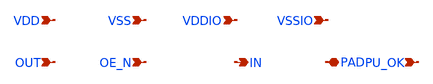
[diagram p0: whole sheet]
** sch_path: sch/pads/gf180mcuD/sdr_bidir_pad.sch
**.subckt sdr_bidir_pad OUT OE_N IN PAD PU_OK VDD VSS VDDIO VSSIO
*.ipin OUT
*.ipin OE_N
*.opin IN
*.iopin PAD
*.ipin PU_OK
*.ipin VDD
*.ipin VSS
*.ipin VDDIO
*.ipin VSSIO
**** begin user architecture code


* GENERATED by generator/emit_pads.py -- DO NOT EDIT BY HAND
* backend: gf180mcuD   pdk: gf180mcuD
* topology: specs/pads/topology.yaml v1 -- ONE shared schematic, only device names change
* STATUS: topology_template_only
* license: Apache-2.0 (GlobalFoundries PDK Authors, design.ngspice header)
* SIZE UNITS: topology params are metres; nfet_03v3/pfet_03v3 take w/l in metres
* ESD NOTE: 2-terminal .model diodes; area unit and orientation still need schematic review
*
* NOT SIMULATABLE. This is a TOPOLOGY TEMPLATE:
*   - every W / L / NF / R / area is an unresolved parameter
*     (see required_params.json). ngspice rejects them until filled.
*   - PAD_OE_CTRL is a generated transistor-level block (IO gates plus
*     an optional core-to-IO level shifter); its devices reuse the
*     pre-driver sizing placeholders and are not optimized.
*   - diode orientation, bulk ties and the series-R third terminal must
*     be confirmed at schematic review; they are NOT signed off here.
*   - L_R_SERIES is the on-chip resistor LENGTH. The target
*     resistance in ohm is a board-level SI input, not a pad param;
*     converting target R to L needs a per-PDK sheet resistance.
*
* Device-instantiation syntax is per backend (nf vs ng, m vs mr,
* r_length/r_width vs w/l, 2-terminal diode model vs 3-terminal ESD
* subckt). It lives in specs/pads/devices/<backend>.yaml; the block
* topology below stays shared.
*
* Expected includes (NOT bundled; integrator supplies models.spice):
*   libs.tech/ngspice/sm141064.ngspice
*   libs.tech/ngspice/design.ngspice
*
* Shared signal chain (docs/ARCHITECTURE.md section 5):
*   OUT/OE_N --[level shift if VDD != VDDIO]--> pre-driver --> tri-state
*   --> series R --> PAD --> ESD (to VDDIO / VSSIO + power clamp)
*   PAD --> CMOS/Schmitt RX --> [level shift back] --> IN
*   power-up Hi-Z until VDD and VDDIO are both present (PU_OK)

X_INV_P Y A VDDIO VDDIO pfet_03v3 w=W_P_PDRV l=L_PDRV nf=NF_DEVICE m=M_DEVICE
X_INV_N Y A VSSIO VSSIO nfet_03v3 w=W_N_PDRV l=L_PDRV nf=NF_DEVICE m=M_DEVICE
X_NAND_P1 Y A VDDIO VDDIO pfet_03v3 w=W_P_PDRV l=L_PDRV nf=NF_DEVICE m=M_DEVICE
X_NAND_P2 Y B VDDIO VDDIO pfet_03v3 w=W_P_PDRV l=L_PDRV nf=NF_DEVICE m=M_DEVICE
X_NAND_N1 Y A nand_mid VSSIO nfet_03v3 w=W_N_PDRV l=L_PDRV nf=NF_DEVICE m=M_DEVICE
X_NAND_N2 nand_mid B VSSIO VSSIO nfet_03v3 w=W_N_PDRV l=L_PDRV nf=NF_DEVICE m=M_DEVICE
X_NOR_P1 Y A nor_mid VDDIO pfet_03v3 w=W_P_PDRV l=L_PDRV nf=NF_DEVICE m=M_DEVICE
X_NOR_P2 nor_mid B VDDIO VDDIO pfet_03v3 w=W_P_PDRV l=L_PDRV nf=NF_DEVICE m=M_DEVICE
X_NOR_N1 Y A VSSIO VSSIO nfet_03v3 w=W_N_PDRV l=L_PDRV nf=NF_DEVICE m=M_DEVICE
X_NOR_N2 Y B VSSIO VSSIO nfet_03v3 w=W_N_PDRV l=L_PDRV nf=NF_DEVICE m=M_DEVICE
* core_v == vddio_v: OUT is already IO domain
V_OUT_I OUT_I OUT 0
X_INV_O OUT OUTB_I VDDIO VSSIO INV_IO
* OE_N and PU_OK are IO-domain control inputs in this macro
X_INV_OE OE_N OENB VDDIO VSSIO INV_IO
X_NAND PU_OK OENB EN_N VDDIO VSSIO NAND2_IO
X_NOR_GN EN_N OUT_I N_GN VDDIO VSSIO NOR2_IO
X_NOR_GP EN_N OUTB_I NGPB VDDIO VSSIO NOR2_IO
X_INV_NGP NGPB N_GP VDDIO VSSIO INV_IO

* --- core_v == vddio_v: NO level shifter (Nominal core and IO voltages are equal; ARCHITECTURE.md
*+ section 5.1 says no level shift. Pre-driver still required.) ---
* OUT / OE_N are already at IO-domain levels; pre-driver still required.

* --- OE / power-up gating: real transistor-level block (see header) ---
X_OE_CTRL n_gp n_gn OUT OE_N PU_OK VDD VSS VDDIO VSSIO PAD_OE_CTRL

* --- pre-driver chain (even stage count preserves polarity) ---
X_PDRV_P_GP1 n_gp_s1 n_gp VDDIO VDDIO pfet_03v3 w=W_P_PDRV l=L_PDRV nf=NF_DEVICE m=M_DEVICE
X_PDRV_N_GP1 n_gp_s1 n_gp VSSIO VSSIO nfet_03v3 w=W_N_PDRV l=L_PDRV nf=NF_DEVICE m=M_DEVICE
X_PDRV_P_GP2 n_gp_drv n_gp_s1 VDDIO VDDIO pfet_03v3 w=W_P_PDRV l=L_PDRV nf=NF_DEVICE m=M_DEVICE
X_PDRV_N_GP2 n_gp_drv n_gp_s1 VSSIO VSSIO nfet_03v3 w=W_N_PDRV l=L_PDRV nf=NF_DEVICE m=M_DEVICE
X_PDRV_P_GN1 n_gn_s1 n_gn VDDIO VDDIO pfet_03v3 w=W_P_PDRV l=L_PDRV nf=NF_DEVICE m=M_DEVICE
X_PDRV_N_GN1 n_gn_s1 n_gn VSSIO VSSIO nfet_03v3 w=W_N_PDRV l=L_PDRV nf=NF_DEVICE m=M_DEVICE
X_PDRV_P_GN2 n_gn_drv n_gn_s1 VDDIO VDDIO pfet_03v3 w=W_P_PDRV l=L_PDRV nf=NF_DEVICE m=M_DEVICE
X_PDRV_N_GN2 n_gn_drv n_gn_s1 VSSIO VSSIO nfet_03v3 w=W_N_PDRV l=L_PDRV nf=NF_DEVICE m=M_DEVICE

* --- tri-state output (PMOS to VDDIO, NMOS to VSSIO) ---
X_OUT_P n_pre n_gp_drv VDDIO VDDIO pfet_03v3 w=W_P_OUT l=L_P_OUT nf=NF_P_OUT m=M_DEVICE
X_OUT_N n_pre n_gn_drv VSSIO VSSIO nfet_03v3 w=W_N_OUT l=L_N_OUT nf=NF_N_OUT m=M_DEVICE

* --- on-chip series damping resistor (may instead live on the board) ---
X_RSER n_pre PAD VSSIO ppolyf_u r_length=L_R_SERIES r_width=W_R_SERIES

* --- ESD: primary diodes + VDDIO-to-VSSIO clamp ---
D_ESD_UP PAD VDDIO diode_pd2nw_03v3 area=ESD_AREA_UP
D_ESD_DN VSSIO PAD diode_nd2ps_03v3 area=ESD_AREA_DN
D_CLAMP VSSIO VDDIO diode_pd2nw_03v3 area=ESD_CLAMP_W

* --- SDR receiver: thick-oxide CMOS inverter (Schmitt optional) ---
X_RX_N IN PAD VSSIO VSSIO nfet_03v3 w=W_RX_N l=L_PDRV nf=NF_DEVICE m=M_DEVICE
X_RX_P IN PAD VDDIO VDDIO pfet_03v3 w=W_RX_P l=L_PDRV nf=NF_DEVICE m=M_DEVICE
* RX_HYST unresolved; do NOT assume the input threshold equals VDDIO/2.


* --- guard ring surrounds output stage and ESD (layout only) ---
* GUARD_RING_WIDTH / GUARD_RING_SPACING unresolved; not drawn here.


**** end user architecture code
**.ends
.end
